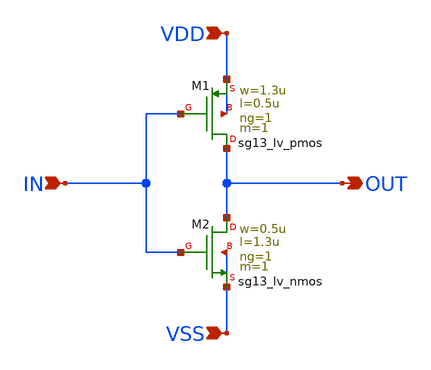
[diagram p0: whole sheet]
** sch_path: 10_xschem/inverter.sch
**.subckt inverter VDD VSS IN OUT
*.ipin VDD
*.ipin VSS
*.ipin IN
*.opin OUT
XM1 OUT IN VDD VDD sg13_lv_pmos w=1.3u l=0.5u ng=1 m=1 mm_ok=1
XM2 OUT IN VSS VSS sg13_lv_nmos w=0.5u l=1.3u ng=1 m=1 mm_ok=1
**.ends
.end
